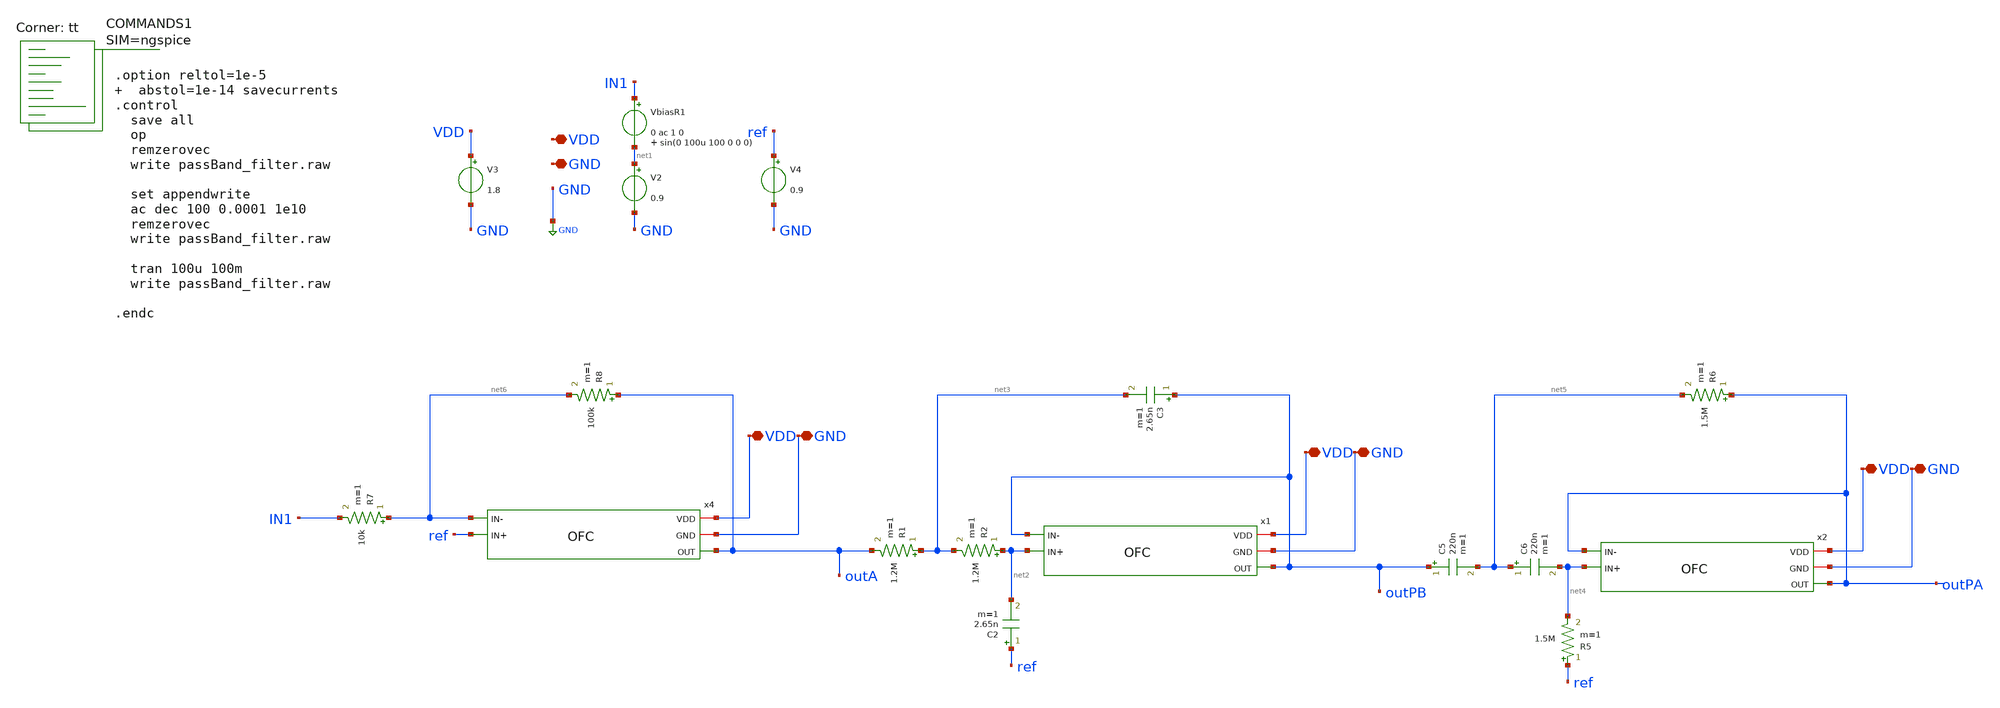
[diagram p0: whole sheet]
** sch_path: xschem/passBand_filter.sch
**.subckt passBand_filter VDD GND VDD GND VDD GND VDD GND
*.iopin VDD
*.iopin GND
*.iopin VDD
*.iopin GND
*.iopin VDD
*.iopin GND
*.iopin VDD
*.iopin GND
V3 VDD GND 1.8
VbiasR1 IN1 net1 0 ac 1 0 sin(0 100u 100 0 0 0)
V2 net1 GND 0.9
V4 ref GND 0.9
x1 VDD GND outPB outPB net2 OFC
R1 net3 outA 1.2M m=1
C2 ref net2 2.65n m=1
R2 net2 net3 1.2M m=1
C3 outPB net3 2.65n m=1
x2 VDD GND outPA outPA net4 OFC
R5 ref net4 1.5M m=1
C5 outPB net5 220n m=1
R6 outPA net5 1.5M m=1
C6 net5 net4 220n m=1
x4 VDD GND outA net6 ref OFC
R8 outA net6 100k m=1
R7 net6 IN1 10k m=1
**** begin user architecture code



.option reltol=1e-5   abstol=1e-14 savecurrents
.control
  save all
  op
  remzerovec
  write passBand_filter.raw

  set appendwrite
  ac dec 100 0.0001 1e10
  remzerovec
  write passBand_filter.raw

  tran 100u 100m
  write passBand_filter.raw

.endc



.lib $::SKYWATER_MODELS/sky130.lib.spice tt
**** end user architecture code
**.ends

* expanding   symbol:  OFC.sym # of pins=5
** sym_path: OFC.sym
** sch_path: OFC.sch
.subckt OFC VDD GND OUT IN- IN+
*.iopin VDD
*.iopin GND
*.ipin IN+
*.ipin IN-
*.opin OUT
XM11 S Vb VDD VDD sky130_fd_pr__pfet_01v8_lvt L=1 W=60 nf=2 ad='int((nf+1)/2) * W/nf * 0.29' as='int((nf+2)/2) * W/nf * 0.29'
+ pd='2*int((nf+1)/2) * (W/nf + 0.29)' ps='2*int((nf+2)/2) * (W/nf + 0.29)' nrd='0.29 / W' nrs='0.29 / W'
+ sa=0 sb=0 sd=0 mult=2 m=2
XM1 D1 IN+ S S sky130_fd_pr__pfet_01v8_lvt L=10 W=25 nf=2 ad='int((nf+1)/2) * W/nf * 0.29' as='int((nf+2)/2) * W/nf * 0.29'
+ pd='2*int((nf+1)/2) * (W/nf + 0.29)' ps='2*int((nf+2)/2) * (W/nf + 0.29)' nrd='0.29 / W' nrs='0.29 / W'
+ sa=0 sb=0 sd=0 mult=2 m=2
XM2 D2 IN- S S sky130_fd_pr__pfet_01v8_lvt L=10 W=25 nf=2 ad='int((nf+1)/2) * W/nf * 0.29' as='int((nf+2)/2) * W/nf * 0.29'
+ pd='2*int((nf+1)/2) * (W/nf + 0.29)' ps='2*int((nf+2)/2) * (W/nf + 0.29)' nrd='0.29 / W' nrs='0.29 / W'
+ sa=0 sb=0 sd=0 mult=2 m=2
XM3 OUT Vc1 D2 GND sky130_fd_pr__nfet_01v8_lvt L=1 W=4 nf=1 ad='int((nf+1)/2) * W/nf * 0.29' as='int((nf+2)/2) * W/nf * 0.29'
+ pd='2*int((nf+1)/2) * (W/nf + 0.29)' ps='2*int((nf+2)/2) * (W/nf + 0.29)' nrd='0.29 / W' nrs='0.29 / W'
+ sa=0 sb=0 sd=0 mult=1 m=1
XM4 D2 Vc GND GND sky130_fd_pr__nfet_01v8_lvt L=1 W=2.8 nf=1 ad='int((nf+1)/2) * W/nf * 0.29' as='int((nf+2)/2) * W/nf * 0.29'
+ pd='2*int((nf+1)/2) * (W/nf + 0.29)' ps='2*int((nf+2)/2) * (W/nf + 0.29)' nrd='0.29 / W' nrs='0.29 / W'
+ sa=0 sb=0 sd=0 mult=1 m=1
XM5 D1 Vc GND GND sky130_fd_pr__nfet_01v8_lvt L=1 W=2.8 nf=1 ad='int((nf+1)/2) * W/nf * 0.29' as='int((nf+2)/2) * W/nf * 0.29'
+ pd='2*int((nf+1)/2) * (W/nf + 0.29)' ps='2*int((nf+2)/2) * (W/nf + 0.29)' nrd='0.29 / W' nrs='0.29 / W'
+ sa=0 sb=0 sd=0 mult=1 m=1
XM6 G Vc1 D1 GND sky130_fd_pr__nfet_01v8_lvt L=1 W=4 nf=1 ad='int((nf+1)/2) * W/nf * 0.29' as='int((nf+2)/2) * W/nf * 0.29'
+ pd='2*int((nf+1)/2) * (W/nf + 0.29)' ps='2*int((nf+2)/2) * (W/nf + 0.29)' nrd='0.29 / W' nrs='0.29 / W'
+ sa=0 sb=0 sd=0 mult=1 m=1
XM7 G Vc2 D9 D9 sky130_fd_pr__pfet_01v8_lvt L=2.23 W=3 nf=1 ad='int((nf+1)/2) * W/nf * 0.29' as='int((nf+2)/2) * W/nf * 0.29'
+ pd='2*int((nf+1)/2) * (W/nf + 0.29)' ps='2*int((nf+2)/2) * (W/nf + 0.29)' nrd='0.29 / W' nrs='0.29 / W'
+ sa=0 sb=0 sd=0 mult=1 m=1
XM9 D9 G VDD VDD sky130_fd_pr__pfet_01v8_lvt L=2.23 W=4 nf=1 ad='int((nf+1)/2) * W/nf * 0.29' as='int((nf+2)/2) * W/nf * 0.29'
+ pd='2*int((nf+1)/2) * (W/nf + 0.29)' ps='2*int((nf+2)/2) * (W/nf + 0.29)' nrd='0.29 / W' nrs='0.29 / W'
+ sa=0 sb=0 sd=0 mult=1 m=1
XM8 D10 G VDD VDD sky130_fd_pr__pfet_01v8_lvt L=2.23 W=4 nf=1 ad='int((nf+1)/2) * W/nf * 0.29' as='int((nf+2)/2) * W/nf * 0.29'
+ pd='2*int((nf+1)/2) * (W/nf + 0.29)' ps='2*int((nf+2)/2) * (W/nf + 0.29)' nrd='0.29 / W' nrs='0.29 / W'
+ sa=0 sb=0 sd=0 mult=1 m=1
XM10 OUT Vc2 D10 D10 sky130_fd_pr__pfet_01v8_lvt L=2.23 W=3 nf=1 ad='int((nf+1)/2) * W/nf * 0.29' as='int((nf+2)/2) * W/nf * 0.29'
+ pd='2*int((nf+1)/2) * (W/nf + 0.29)' ps='2*int((nf+2)/2) * (W/nf + 0.29)' nrd='0.29 / W' nrs='0.29 / W'
+ sa=0 sb=0 sd=0 mult=1 m=1
XR2 Vb VDD GND sky130_fd_pr__res_xhigh_po_0p35 L=5 mult=1 m=1
XR3 GND Vb GND sky130_fd_pr__res_xhigh_po_0p35 L=13.2 mult=1 m=1
XR1 Vc VDD GND sky130_fd_pr__res_xhigh_po_0p35 L=5 mult=1 m=1
XR4 GND Vc GND sky130_fd_pr__res_xhigh_po_0p35 L=3.07 mult=1 m=1
XR5 Vc1 VDD GND sky130_fd_pr__res_xhigh_po_0p35 L=5 mult=1 m=1
XR6 GND Vc1 GND sky130_fd_pr__res_xhigh_po_0p35 L=13.2 mult=1 m=1
XR7 Vc2 VDD GND sky130_fd_pr__res_xhigh_po_0p35 L=5 mult=1 m=1
XR8 GND Vc2 GND sky130_fd_pr__res_xhigh_po_0p35 L=1.6 mult=1 m=1
.ends

.GLOBAL GND
.end
